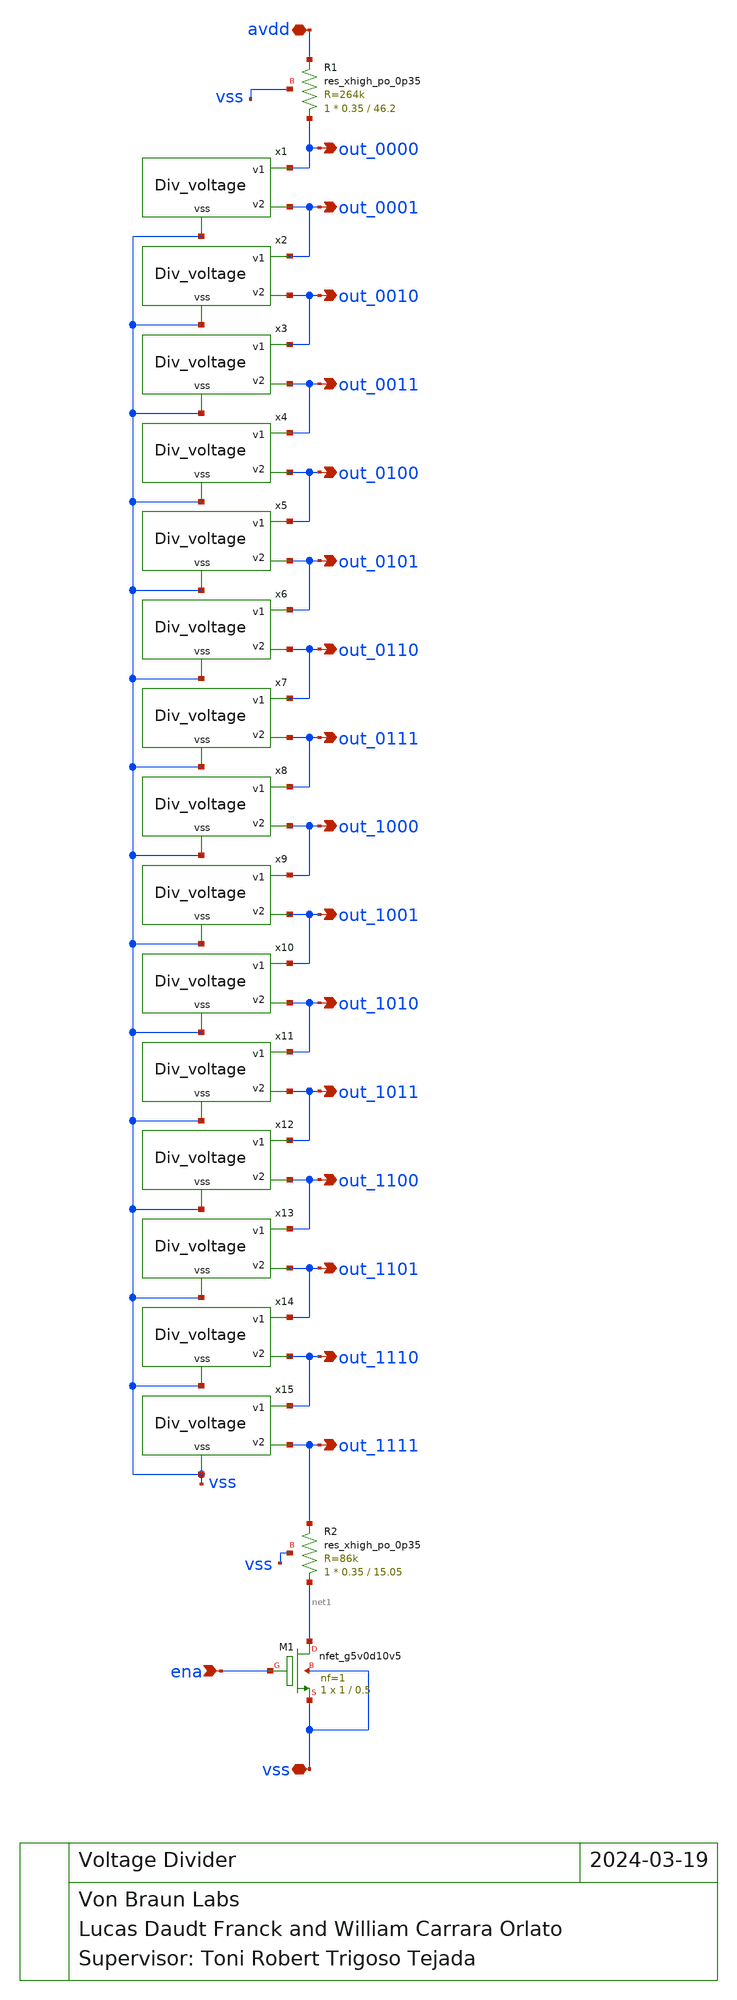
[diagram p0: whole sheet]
** sch_path: xschem/divisor_completo.sch
**.subckt divisor_completo ena vss avdd out_1110 out_1101 out_1100 out_1011 out_1010 out_1001
*+ out_1000 out_0000 out_0001 out_0010 out_0011 out_0100 out_0101 out_0110 out_0111 out_1111
*.ipin ena
*.iopin vss
*.iopin avdd
*.opin out_1110
*.opin out_1101
*.opin out_1100
*.opin out_1011
*.opin out_1010
*.opin out_1001
*.opin out_1000
*.opin out_0000
*.opin out_0001
*.opin out_0010
*.opin out_0011
*.opin out_0100
*.opin out_0101
*.opin out_0110
*.opin out_0111
*.opin out_1111
x1 out_0000 out_0001 vss div_voltage
x2 out_0001 out_0010 vss div_voltage
x3 out_0010 out_0011 vss div_voltage
x4 out_0011 out_0100 vss div_voltage
x5 out_0100 out_0101 vss div_voltage
x6 out_0101 out_0110 vss div_voltage
x7 out_0110 out_0111 vss div_voltage
x8 out_0111 out_1000 vss div_voltage
x9 out_1000 out_1001 vss div_voltage
x10 out_1001 out_1010 vss div_voltage
x11 out_1010 out_1011 vss div_voltage
x12 out_1011 out_1100 vss div_voltage
x13 out_1100 out_1101 vss div_voltage
x14 out_1101 out_1110 vss div_voltage
x15 out_1110 out_1111 vss div_voltage
XR1 out_0000 avdd vss sky130_fd_pr__res_xhigh_po_0p35 L=46.2 mult=1 m=1
XR2 net1 out_1111 vss sky130_fd_pr__res_xhigh_po_0p35 L=15.05 mult=1 m=1
XM1 net1 ena vss vss sky130_fd_pr__nfet_g5v0d10v5 L=0.5 W=1 nf=1 ad='int((nf+1)/2) * W/nf * 0.29' as='int((nf+2)/2) * W/nf * 0.29'
+ pd='2*int((nf+1)/2) * (W/nf + 0.29)' ps='2*int((nf+2)/2) * (W/nf + 0.29)' nrd='0.29 / W' nrs='0.29 / W'
+ sa=0 sb=0 sd=0 mult=1 m=1
**.ends

* expanding   symbol:  div_voltage.sym # of pins=3
** sym_path: blocks/input/xschem/div_voltage.sym
** sch_path: blocks/input/xschem/div_voltage.sch
.subckt div_voltage v1 v2 vss
*.iopin vss
*.iopin v1
*.iopin v2
R1 v1 net1 4k m=1
R2 net1 v2 4k m=1
.ends

.end
